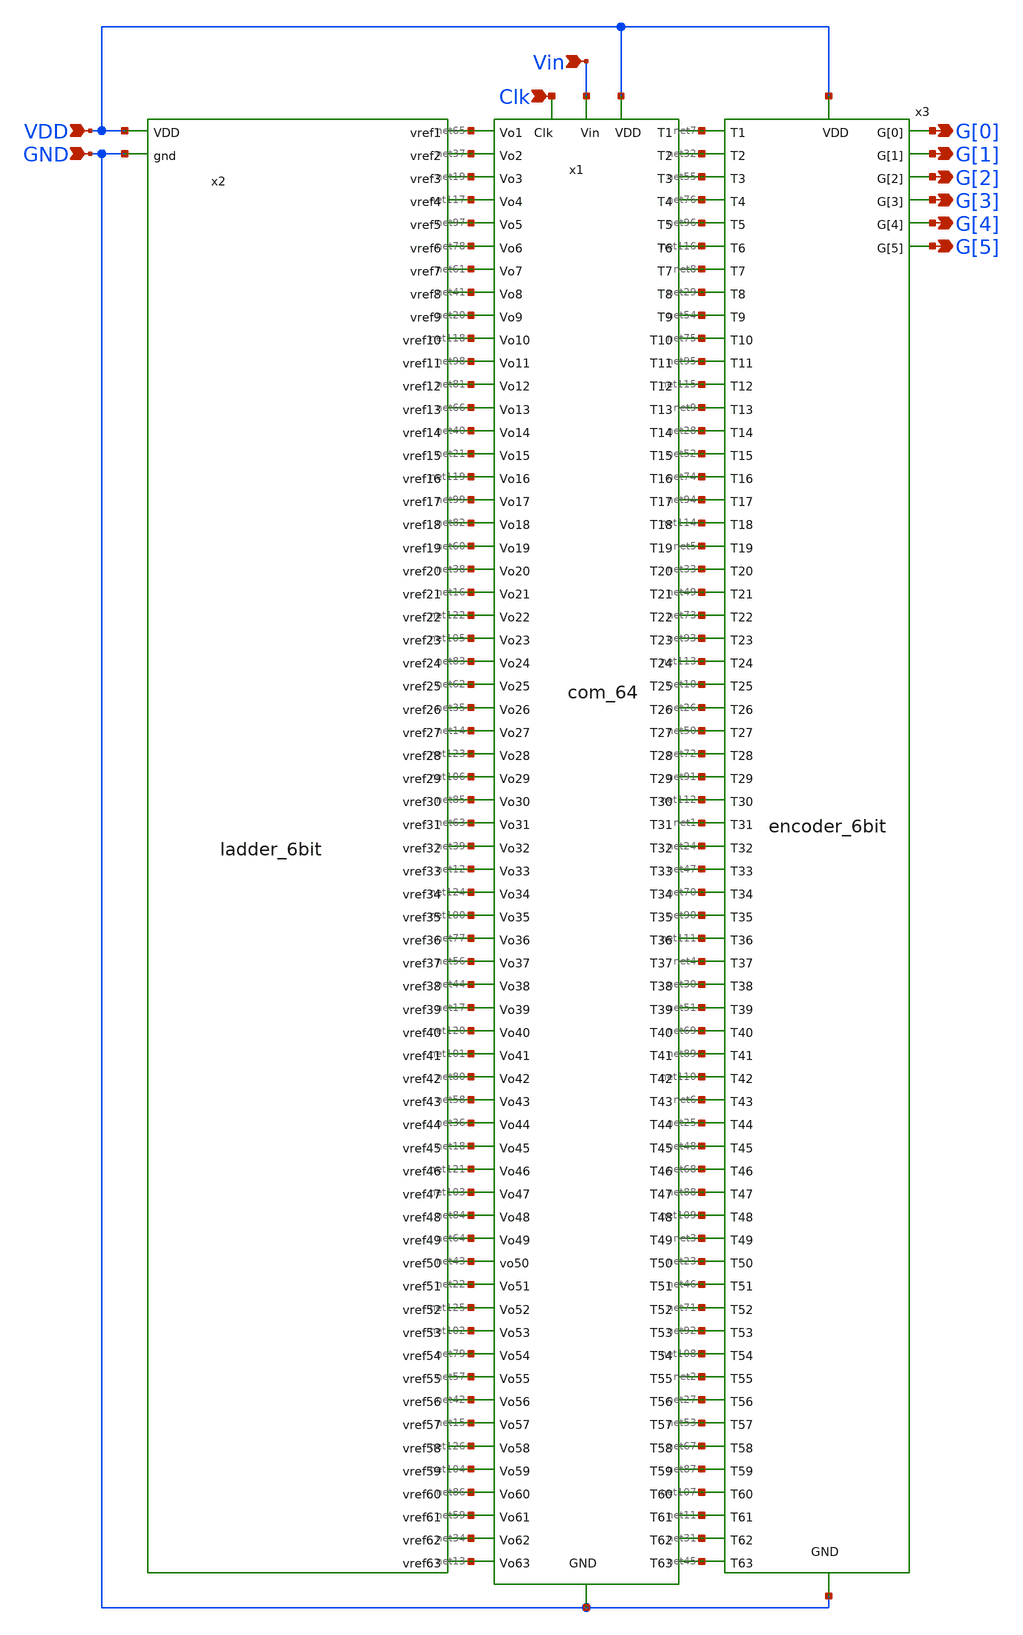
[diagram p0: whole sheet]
** sch_path: ADC_6bit.sch
**.subckt ADC_6bit VDD GND Clk G[2] G[0] G[3] G[1] G[5] G[4] Vin
*.ipin VDD
*.ipin GND
*.ipin Clk
*.opin G[2]
*.opin G[0]
*.opin G[3]
*.opin G[1]
*.opin G[5]
*.opin G[4]
*.ipin Vin
x1 VDD Vin Clk net1 net2 net3 net4 net5 net6 net7 net8 net9 net10 net11 net12 net13 net14 net15
+ net16 net17 net18 net19 net20 net21 net22 net23 net24 net25 net26 net27 net28 net29 net30 net31 net32
+ net33 net34 net35 net36 net37 net38 net39 net40 net41 net42 net43 net44 net45 net46 net47 net48 net49
+ net50 net51 net52 net53 net54 net55 net56 net57 net58 net59 net60 net61 net62 net63 net64 net65 net66
+ net67 net68 net69 net70 net71 net72 net73 net74 net75 net76 net77 net78 net79 net80 net81 net82 net83
+ net84 net85 net86 net87 net88 net89 net90 net91 net92 net93 net94 net95 net96 net97 net98 net99 net100
+ net101 net102 net103 net104 net105 net106 net107 net108 net109 net110 net111 net112 net113 net114 net115
+ net116 net117 net118 net119 net120 net121 net122 net123 net124 net125 net126 GND com_64
x3 VDD net32 net7 GND net55 G[2] net76 net96 G[0] net116 G[3] net8 G[1] G[5] net29 net54 G[4] net75
+ net95 net115 net9 net28 net52 net74 net94 net114 net5 net33 net49 net73 net93 net113 net10 net26 net50
+ net72 net91 net112 net1 net24 net47 net70 net90 net111 net4 net30 net51 net69 net89 net110 net6 net25
+ net48 net68 net88 net109 net3 net23 net46 net71 net92 net108 net2 net27 net53 net67 net87 net107 net11
+ net31 net45 encoder_6bit
x2 VDD net39 net84 net119 net65 net12 net99 net64 net63 net103 net21 net13 net37 net124 net43 net82
+ net85 net40 net34 net121 net19 net22 net100 net60 net106 net66 net18 net59 net117 net125 net38 net77
+ net86 net123 net36 net81 net56 net16 net97 net102 net98 net104 net58 net14 net44 net78 net79 net122
+ net126 net80 net35 net118 net17 net105 net61 net57 net20 net15 net62 net101 net120 net83 net41 net42 GND
+ ladder_6bit
**.ends
.end
